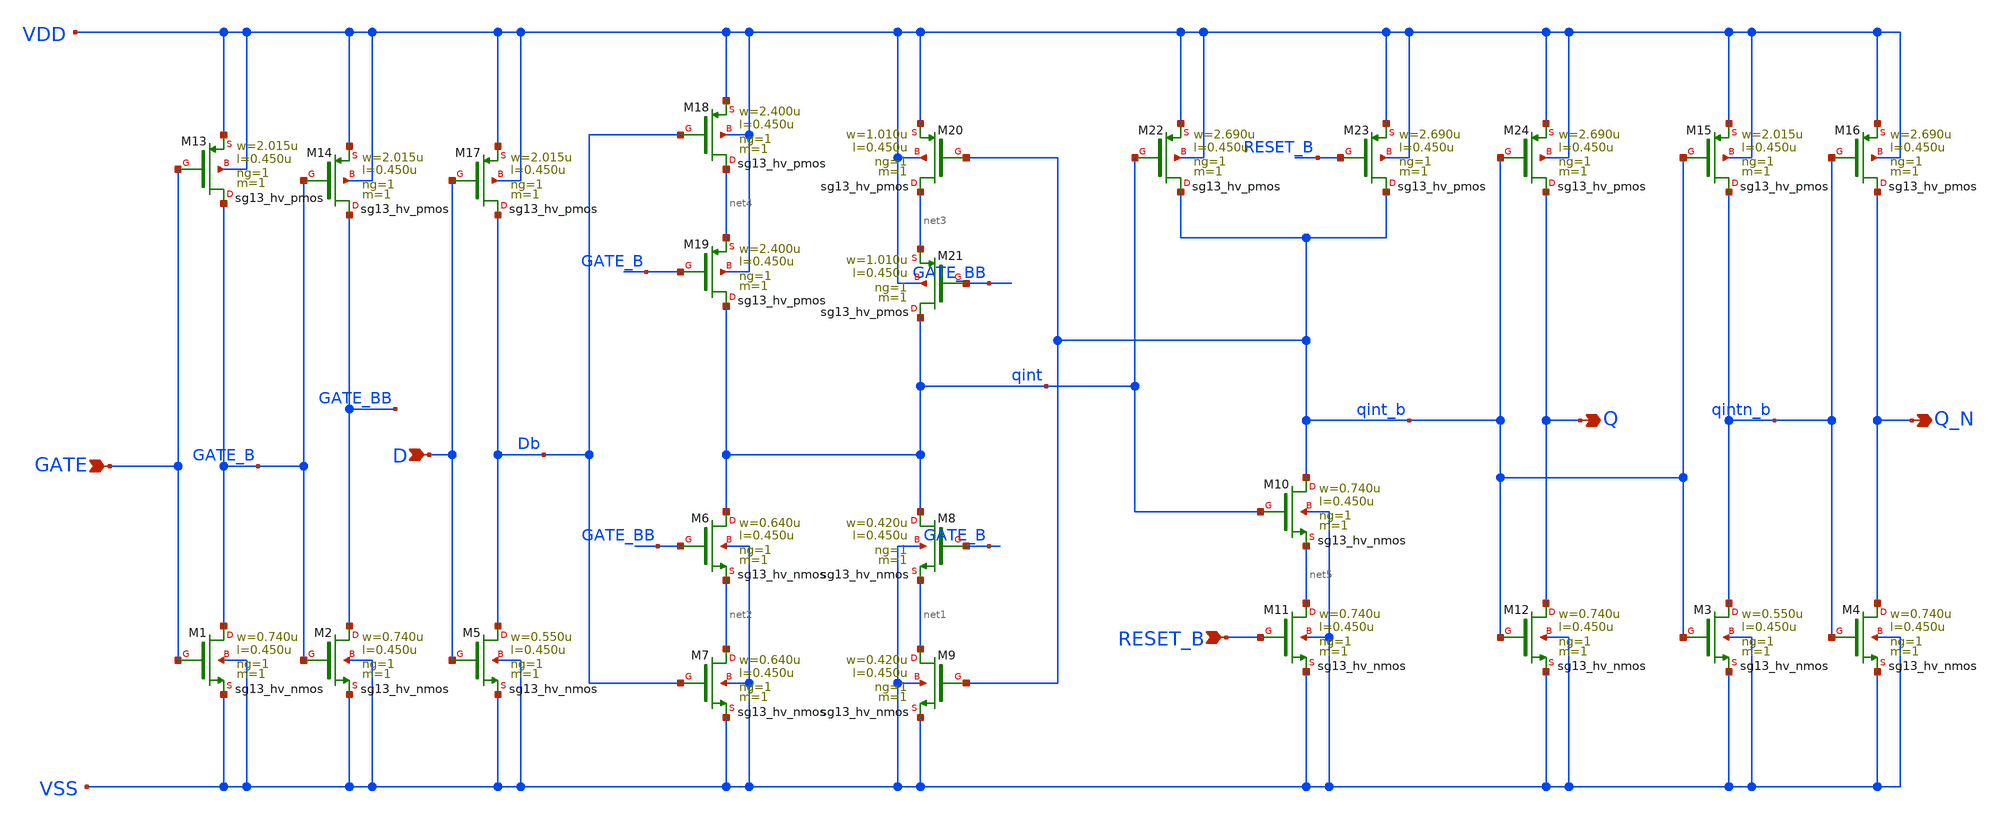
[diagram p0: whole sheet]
** sch_path: ihp-sg13g2/libs.ref/sg13g2_stdcell_hv/sch/xschem/sg13g2_hv_dlhr_1.sch
* Copyright 2023 IHP PDK Authors
* Licensed under the Apache License, Version 2.0 (the "License");
* you may not use this file except in compliance with the License.
* You may obtain a copy of the License at
* https://www.apache.org/licenses/LICENSE-2.0
* Unless required by applicable law or agreed to in writing, software
* distributed under the License is distributed on an "AS IS" BASIS,
* WITHOUT WARRANTIES OR CONDITIONS OF ANY KIND, either express or implied.
* See the License for the specific language governing permissions and
* limitations under the License.
**.subckt sg13g2_hv_dlhr_1 D GATE RESET_B Q Q_N
*.ipin D
*.ipin GATE
*.ipin RESET_B
*.opin Q
*.opin Q_N
XM1 GATE_B GATE VSS VSS sg13_hv_nmos w=0.740u l=0.450u ng=1 m=1 mm_ok=1
XM2 GATE_BB GATE_B VSS VSS sg13_hv_nmos w=0.740u l=0.450u ng=1 m=1 mm_ok=1
XM3 qintn_b qint_b VSS VSS sg13_hv_nmos w=0.550u l=0.450u ng=1 m=1 mm_ok=1
XM4 Q_N qintn_b VSS VSS sg13_hv_nmos w=0.740u l=0.450u ng=1 m=1 mm_ok=1
XM5 Db D VSS VSS sg13_hv_nmos w=0.550u l=0.450u ng=1 m=1 mm_ok=1
XM6 qint GATE_BB net2 VSS sg13_hv_nmos w=0.640u l=0.450u ng=1 m=1 mm_ok=1
XM7 net2 Db VSS VSS sg13_hv_nmos w=0.640u l=0.450u ng=1 m=1 mm_ok=1
XM8 qint GATE_B net1 VSS sg13_hv_nmos w=0.420u l=0.450u ng=1 m=1 mm_ok=1
XM9 net1 qint_b VSS VSS sg13_hv_nmos w=0.420u l=0.450u ng=1 m=1 mm_ok=1
XM10 qint_b qint net5 VSS sg13_hv_nmos w=0.740u l=0.450u ng=1 m=1 mm_ok=1
XM11 net5 RESET_B VSS VSS sg13_hv_nmos w=0.740u l=0.450u ng=1 m=1 mm_ok=1
XM12 Q qint_b VSS VSS sg13_hv_nmos w=0.740u l=0.450u ng=1 m=1 mm_ok=1
XM13 GATE_B GATE VDD VDD sg13_hv_pmos w=2.015u l=0.450u ng=1 m=1 mm_ok=1
XM14 GATE_BB GATE_B VDD VDD sg13_hv_pmos w=2.015u l=0.450u ng=1 m=1 mm_ok=1
XM15 qintn_b qint_b VDD VDD sg13_hv_pmos w=2.015u l=0.450u ng=1 m=1 mm_ok=1
XM16 Q_N qintn_b VDD VDD sg13_hv_pmos w=2.690u l=0.450u ng=1 m=1 mm_ok=1
XM17 Db D VDD VDD sg13_hv_pmos w=2.015u l=0.450u ng=1 m=1 mm_ok=1
XM18 net4 Db VDD VDD sg13_hv_pmos w=2.400u l=0.450u ng=1 m=1 mm_ok=1
XM19 qint GATE_B net4 VDD sg13_hv_pmos w=2.400u l=0.450u ng=1 m=1 mm_ok=1
XM20 net3 qint_b VDD VDD sg13_hv_pmos w=1.010u l=0.450u ng=1 m=1 mm_ok=1
XM21 qint GATE_BB net3 VDD sg13_hv_pmos w=1.010u l=0.450u ng=1 m=1 mm_ok=1
XM22 qint_b qint VDD VDD sg13_hv_pmos w=2.690u l=0.450u ng=1 m=1 mm_ok=1
XM23 qint_b RESET_B VDD VDD sg13_hv_pmos w=2.690u l=0.450u ng=1 m=1 mm_ok=1
XM24 Q qint_b VDD VDD sg13_hv_pmos w=2.690u l=0.450u ng=1 m=1 mm_ok=1
**.ends
.end
